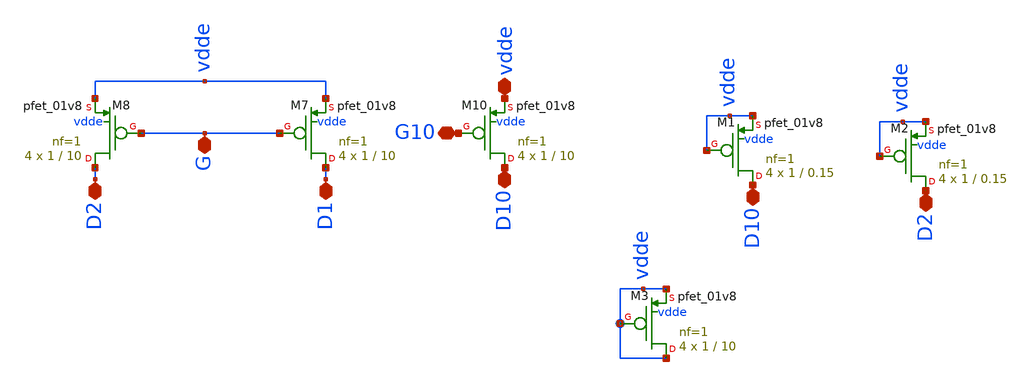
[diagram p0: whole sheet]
** sch_path: magic/pmos_current_bgr.sch
**.subckt pmos_current_bgr vdde G10 D10 D1 D2 D10 D2 G
*.iopin vdde
*.iopin G10
*.iopin D10
*.iopin D1
*.iopin D2
*.iopin D10
*.iopin D2
*.iopin G
XM10 D10 G10 vdde vdde sky130_fd_pr__pfet_01v8 L=10 W=1 nf=1 ad='int((nf+1)/2) * W/nf * 0.29' as='int((nf+2)/2) * W/nf * 0.29'
+ pd='2*int((nf+1)/2) * (W/nf + 0.29)' ps='2*int((nf+2)/2) * (W/nf + 0.29)' nrd='0.29 / W' nrs='0.29 / W'
+ sa=0 sb=0 sd=0 mult=4 m=4
XM7 D1 G vdde vdde sky130_fd_pr__pfet_01v8 L=10 W=1 nf=1 ad='int((nf+1)/2) * W/nf * 0.29' as='int((nf+2)/2) * W/nf * 0.29'
+ pd='2*int((nf+1)/2) * (W/nf + 0.29)' ps='2*int((nf+2)/2) * (W/nf + 0.29)' nrd='0.29 / W' nrs='0.29 / W'
+ sa=0 sb=0 sd=0 mult=4 m=4
XM8 D2 G vdde vdde sky130_fd_pr__pfet_01v8 L=10 W=1 nf=1 ad='int((nf+1)/2) * W/nf * 0.29' as='int((nf+2)/2) * W/nf * 0.29'
+ pd='2*int((nf+1)/2) * (W/nf + 0.29)' ps='2*int((nf+2)/2) * (W/nf + 0.29)' nrd='0.29 / W' nrs='0.29 / W'
+ sa=0 sb=0 sd=0 mult=4 m=4
XM1 D10 vdde vdde vdde sky130_fd_pr__pfet_01v8 L=0.15 W=1 nf=1 ad='int((nf+1)/2) * W/nf * 0.29' as='int((nf+2)/2) * W/nf * 0.29'
+ pd='2*int((nf+1)/2) * (W/nf + 0.29)' ps='2*int((nf+2)/2) * (W/nf + 0.29)' nrd='0.29 / W' nrs='0.29 / W'
+ sa=0 sb=0 sd=0 mult=4 m=4
XM2 D2 vdde vdde vdde sky130_fd_pr__pfet_01v8 L=0.15 W=1 nf=1 ad='int((nf+1)/2) * W/nf * 0.29' as='int((nf+2)/2) * W/nf * 0.29'
+ pd='2*int((nf+1)/2) * (W/nf + 0.29)' ps='2*int((nf+2)/2) * (W/nf + 0.29)' nrd='0.29 / W' nrs='0.29 / W'
+ sa=0 sb=0 sd=0 mult=4 m=4
XM3 vdde vdde vdde vdde sky130_fd_pr__pfet_01v8 L=10 W=1 nf=1 ad='int((nf+1)/2) * W/nf * 0.29' as='int((nf+2)/2) * W/nf * 0.29'
+ pd='2*int((nf+1)/2) * (W/nf + 0.29)' ps='2*int((nf+2)/2) * (W/nf + 0.29)' nrd='0.29 / W' nrs='0.29 / W'
+ sa=0 sb=0 sd=0 mult=4 m=4
**.ends
.end
